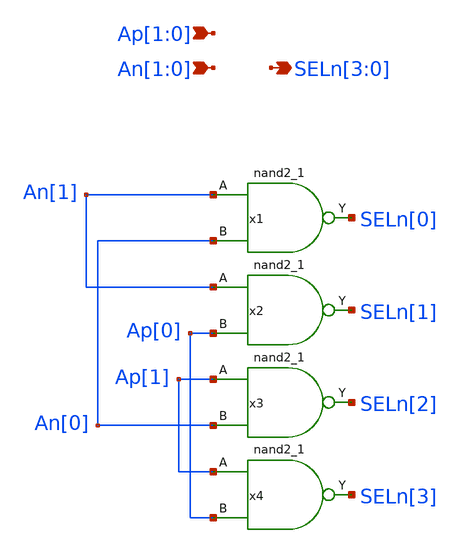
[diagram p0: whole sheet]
** sch_path: blocks/rom/rom_dec_2b.sch
**.subckt rom_dec_2b Ap[1],Ap[0] SELn[3],SELn[2],SELn[1],SELn[0] An[1],An[0]
*.ipin Ap[1],Ap[0]
*.opin SELn[3],SELn[2],SELn[1],SELn[0]
*.ipin An[1],An[0]
x1 An[1] An[0] VSS VSS VCC VCC SELn[0] sky130_fd_sc_hd__nand2_1
x2 An[1] Ap[0] VSS VSS VCC VCC SELn[1] sky130_fd_sc_hd__nand2_1
x3 Ap[1] An[0] VSS VSS VCC VCC SELn[2] sky130_fd_sc_hd__nand2_1
x4 Ap[1] Ap[0] VSS VSS VCC VCC SELn[3] sky130_fd_sc_hd__nand2_1
**.ends
.end
